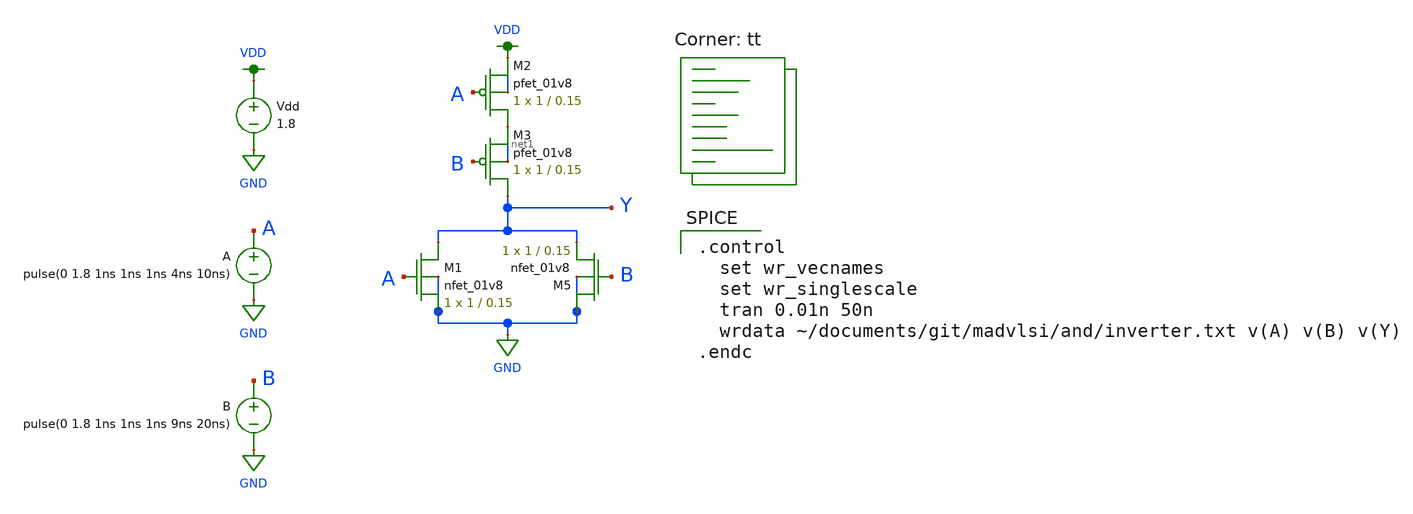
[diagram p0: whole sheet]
** sch_path: and/schematic/nand_tran.sch
**.subckt nand_tran
XM1 Y A GND GND sky130_fd_pr__nfet_01v8 L=0.15 W=1 nf=1 ad='int((nf+1)/2) * W/nf * 0.29' as='int((nf+2)/2) * W/nf * 0.29'
+ pd='2*int((nf+1)/2) * (W/nf + 0.29)' ps='2*int((nf+2)/2) * (W/nf + 0.29)' nrd='0.29 / W' nrs='0.29 / W'
+ sa=0 sb=0 sd=0 mult=1 m=1
XM2 net1 A VDD VDD sky130_fd_pr__pfet_01v8 L=0.15 W=1 nf=1 ad='int((nf+1)/2) * W/nf * 0.29' as='int((nf+2)/2) * W/nf * 0.29'
+ pd='2*int((nf+1)/2) * (W/nf + 0.29)' ps='2*int((nf+2)/2) * (W/nf + 0.29)' nrd='0.29 / W' nrs='0.29 / W'
+ sa=0 sb=0 sd=0 mult=1 m=1
Vdd VDD GND 1.8
A A GND pulse(0 1.8 1ns 1ns 1ns 4ns 10ns)
XM3 Y B net1 net1 sky130_fd_pr__pfet_01v8 L=0.15 W=1 nf=1 ad='int((nf+1)/2) * W/nf * 0.29' as='int((nf+2)/2) * W/nf * 0.29'
+ pd='2*int((nf+1)/2) * (W/nf + 0.29)' ps='2*int((nf+2)/2) * (W/nf + 0.29)' nrd='0.29 / W' nrs='0.29 / W'
+ sa=0 sb=0 sd=0 mult=1 m=1
XM5 GND B Y GND sky130_fd_pr__nfet_01v8 L=0.15 W=1 nf=1 ad='int((nf+1)/2) * W/nf * 0.29' as='int((nf+2)/2) * W/nf * 0.29'
+ pd='2*int((nf+1)/2) * (W/nf + 0.29)' ps='2*int((nf+2)/2) * (W/nf + 0.29)' nrd='0.29 / W' nrs='0.29 / W'
+ sa=0 sb=0 sd=0 mult=1 m=1
B B GND pulse(0 1.8 1ns 1ns 1ns 9ns 20ns)
**** begin user architecture code

.control
  set wr_vecnames
  set wr_singlescale
  tran 0.01n 50n
  wrdata ~/documents/git/madvlsi/and/inverter.txt v(A) v(B) v(Y)
.endc

.lib $::SKYWATER_MODELS/sky130.lib.spice tt
**** end user architecture code
**.ends
.GLOBAL GND
.GLOBAL VDD
.end
